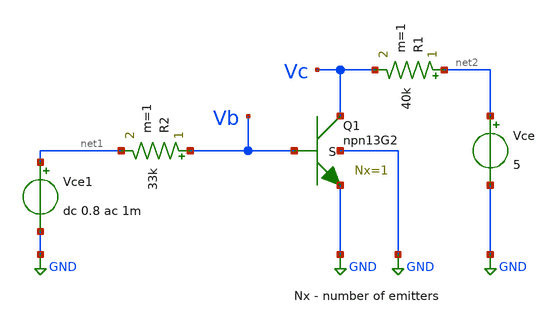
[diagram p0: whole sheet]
** sch_path: ihp-sg13g2/xschem_libs/sg13g2_tests_ase/ac_hbt_13g2/schematic/ac_hbt_13g2.sch
* Copyright 2023 IHP PDK Authors
**.subckt ac_hbt_13g2
Vce net2 GND 5
XQ1 Vc Vb GND GND npn13G2 Nx=1 mm_ok=1
R1 net2 Vc 40k m=1
Vce1 net1 GND dc 0.8 ac 1m
R2 Vb net1 33k m=1
**.ends
.GLOBAL GND
.end
